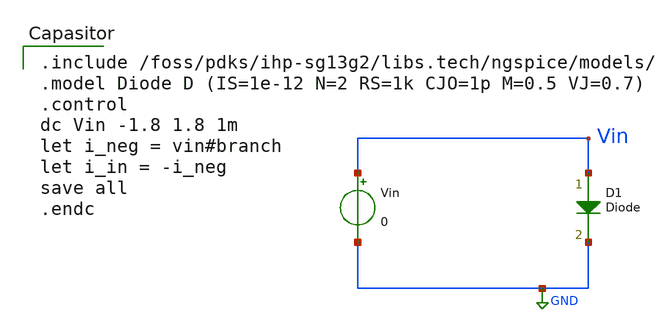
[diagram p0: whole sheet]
** sch_path: content/simulation_files/xschem/04_Diode.sch
**.subckt 04_Diode
Vin Vin GND 0
D1 Vin GND Diode area=1
**** begin user architecture code

.include /foss/pdks/ihp-sg13g2/libs.tech/ngspice/models/
.model Diode D (IS=1e-12 N=2 RS=1k CJO=1p M=0.5 VJ=0.7)
.control
dc Vin -1.8 1.8 1m
let i_neg = vin#branch
let i_in = -i_neg
save all
.endc

**** end user architecture code
**.ends
.GLOBAL GND
.end
